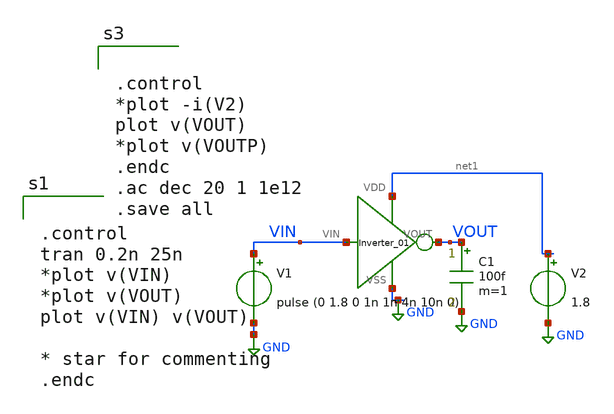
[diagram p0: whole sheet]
** sch_path: xschem/xschem_BGR_Top/Sigma_Delta/Inverter_01/Inverter_01_TB.sch
**.subckt Inverter_01_TB
V1 VIN GND pulse (0 1.8 0 1n 1n 4n 10n 0)
V2 net1 GND 1.8
X1 GND net1 VIN VOUT Inverter_01
C1 VOUT GND 100f m=1
**** begin user architecture code


.control
tran 0.2n 25n
*plot v(VIN)
*plot v(VOUT)
plot v(VIN) v(VOUT)

* star for commenting
.endc


** opencircuitdesign pdks install
.lib $::SKYWATER_MODELS/sky130.lib.spice tt




.control
*plot -i(V2)
plot v(VOUT)
*plot v(VOUTP)
.endc
.ac dec 20 1 1e12
.save all

**** end user architecture code
**.ends

* expanding   symbol:  Sigma_Delta/Inverter_01/Inverter_01.sym # of pins=4
** sym_path: xschem/xschem_BGR_Top/Sigma_Delta/Inverter_01/Inverter_01.sym
** sch_path: xschem/xschem_BGR_Top/Sigma_Delta/Inverter_01/Inverter_01.sch
.subckt Inverter_01 VSS VDD VIN VOUT
*.iopin VIN
*.iopin VDD
*.iopin VSS
*.iopin VOUT
XM1 VOUT VIN VSS VSS sky130_fd_pr__nfet_01v8 L=0.48 W=0.4 nf=1 ad='int((nf+1)/2) * W/nf * 0.29' as='int((nf+2)/2) * W/nf * 0.29'
+ pd='2*int((nf+1)/2) * (W/nf + 0.29)' ps='2*int((nf+2)/2) * (W/nf + 0.29)' nrd='0.29 / W' nrs='0.29 / W'
+ sa=0 sb=0 sd=0 mult=1 m=1
XM2 VOUT VIN VDD VDD sky130_fd_pr__pfet_01v8 L=0.48 W=0.8 nf=1 ad='int((nf+1)/2) * W/nf * 0.29' as='int((nf+2)/2) * W/nf * 0.29'
+ pd='2*int((nf+1)/2) * (W/nf + 0.29)' ps='2*int((nf+2)/2) * (W/nf + 0.29)' nrd='0.29 / W' nrs='0.29 / W'
+ sa=0 sb=0 sd=0 mult=1 m=1
.ends

.GLOBAL GND
.end
